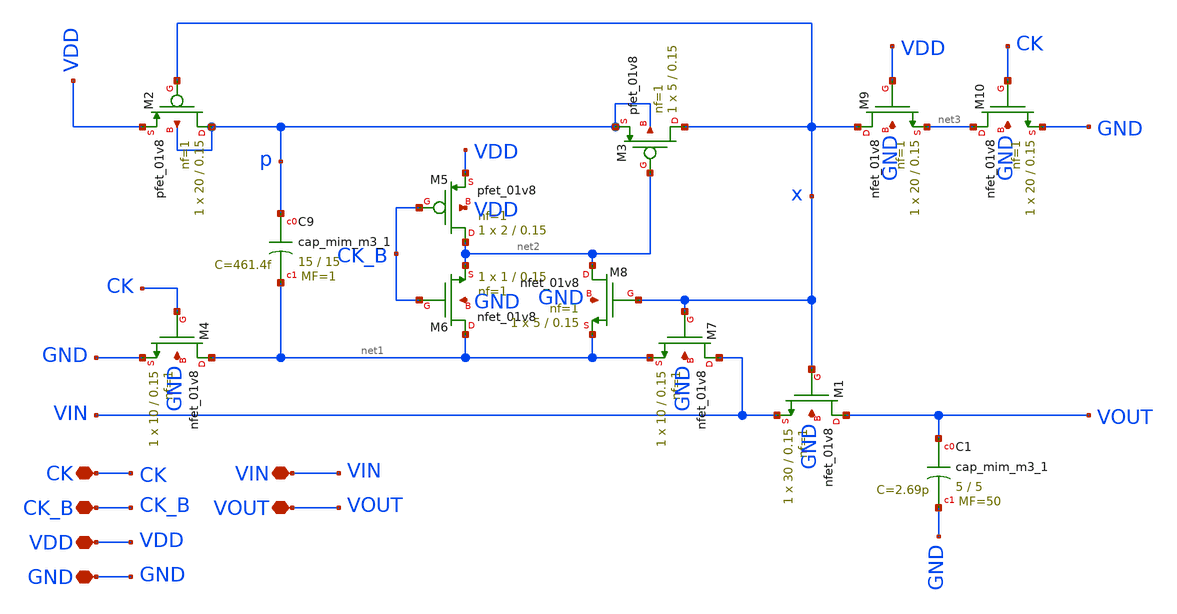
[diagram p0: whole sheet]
** sch_path: xschem/sample/sample_hold.sch
**.subckt sample_hold GND VDD CK CK_B VIN VOUT
*.iopin GND
*.iopin VDD
*.iopin CK
*.iopin CK_B
*.iopin VIN
*.iopin VOUT
XM4 net1 CK GND GND sky130_fd_pr__nfet_01v8 L=0.15 W=10 nf=1 ad='int((nf+1)/2) * W/nf * 0.29' as='int((nf+2)/2) * W/nf * 0.29'
+ pd='2*int((nf+1)/2) * (W/nf + 0.29)' ps='2*int((nf+2)/2) * (W/nf + 0.29)' nrd='0.29 / W' nrs='0.29 / W'
+ sa=0 sb=0 sd=0 mult=1 m=1
XM1 VOUT x VIN GND sky130_fd_pr__nfet_01v8 L=0.15 W=30 nf=1 ad='int((nf+1)/2) * W/nf * 0.29' as='int((nf+2)/2) * W/nf * 0.29'
+ pd='2*int((nf+1)/2) * (W/nf + 0.29)' ps='2*int((nf+2)/2) * (W/nf + 0.29)' nrd='0.29 / W' nrs='0.29 / W'
+ sa=0 sb=0 sd=0 mult=1 m=1
XM2 p x VDD p sky130_fd_pr__pfet_01v8 L=0.15 W=20 nf=1 ad='int((nf+1)/2) * W/nf * 0.29' as='int((nf+2)/2) * W/nf * 0.29'
+ pd='2*int((nf+1)/2) * (W/nf + 0.29)' ps='2*int((nf+2)/2) * (W/nf + 0.29)' nrd='0.29 / W' nrs='0.29 / W'
+ sa=0 sb=0 sd=0 mult=1 m=1
XM3 x net2 p p sky130_fd_pr__pfet_01v8 L=0.15 W=5 nf=1 ad='int((nf+1)/2) * W/nf * 0.29' as='int((nf+2)/2) * W/nf * 0.29'
+ pd='2*int((nf+1)/2) * (W/nf + 0.29)' ps='2*int((nf+2)/2) * (W/nf + 0.29)' nrd='0.29 / W' nrs='0.29 / W'
+ sa=0 sb=0 sd=0 mult=1 m=1
XM5 net2 CK_B VDD VDD sky130_fd_pr__pfet_01v8 L=0.15 W=2 nf=1 ad='int((nf+1)/2) * W/nf * 0.29' as='int((nf+2)/2) * W/nf * 0.29'
+ pd='2*int((nf+1)/2) * (W/nf + 0.29)' ps='2*int((nf+2)/2) * (W/nf + 0.29)' nrd='0.29 / W' nrs='0.29 / W'
+ sa=0 sb=0 sd=0 mult=1 m=1
XM6 net1 CK_B net2 GND sky130_fd_pr__nfet_01v8 L=0.15 W=1 nf=1 ad='int((nf+1)/2) * W/nf * 0.29' as='int((nf+2)/2) * W/nf * 0.29'
+ pd='2*int((nf+1)/2) * (W/nf + 0.29)' ps='2*int((nf+2)/2) * (W/nf + 0.29)' nrd='0.29 / W' nrs='0.29 / W'
+ sa=0 sb=0 sd=0 mult=1 m=1
XM7 VIN x net1 GND sky130_fd_pr__nfet_01v8 L=0.15 W=10 nf=1 ad='int((nf+1)/2) * W/nf * 0.29' as='int((nf+2)/2) * W/nf * 0.29'
+ pd='2*int((nf+1)/2) * (W/nf + 0.29)' ps='2*int((nf+2)/2) * (W/nf + 0.29)' nrd='0.29 / W' nrs='0.29 / W'
+ sa=0 sb=0 sd=0 mult=1 m=1
XM8 net2 x net1 GND sky130_fd_pr__nfet_01v8 L=0.15 W=5 nf=1 ad='int((nf+1)/2) * W/nf * 0.29' as='int((nf+2)/2) * W/nf * 0.29'
+ pd='2*int((nf+1)/2) * (W/nf + 0.29)' ps='2*int((nf+2)/2) * (W/nf + 0.29)' nrd='0.29 / W' nrs='0.29 / W'
+ sa=0 sb=0 sd=0 mult=1 m=1
XM9 x VDD net3 GND sky130_fd_pr__nfet_01v8 L=0.15 W=20 nf=1 ad='int((nf+1)/2) * W/nf * 0.29' as='int((nf+2)/2) * W/nf * 0.29'
+ pd='2*int((nf+1)/2) * (W/nf + 0.29)' ps='2*int((nf+2)/2) * (W/nf + 0.29)' nrd='0.29 / W' nrs='0.29 / W'
+ sa=0 sb=0 sd=0 mult=1 m=1
XM10 net3 CK GND GND sky130_fd_pr__nfet_01v8 L=0.15 W=20 nf=1 ad='int((nf+1)/2) * W/nf * 0.29' as='int((nf+2)/2) * W/nf * 0.29'
+ pd='2*int((nf+1)/2) * (W/nf + 0.29)' ps='2*int((nf+2)/2) * (W/nf + 0.29)' nrd='0.29 / W' nrs='0.29 / W'
+ sa=0 sb=0 sd=0 mult=1 m=1
XC9 p net1 sky130_fd_pr__cap_mim_m3_1 W=15 L=15 MF=1 m=1
XC1 VOUT GND sky130_fd_pr__cap_mim_m3_1 W=5 L=5 MF=50 m=50
**.ends
.end
